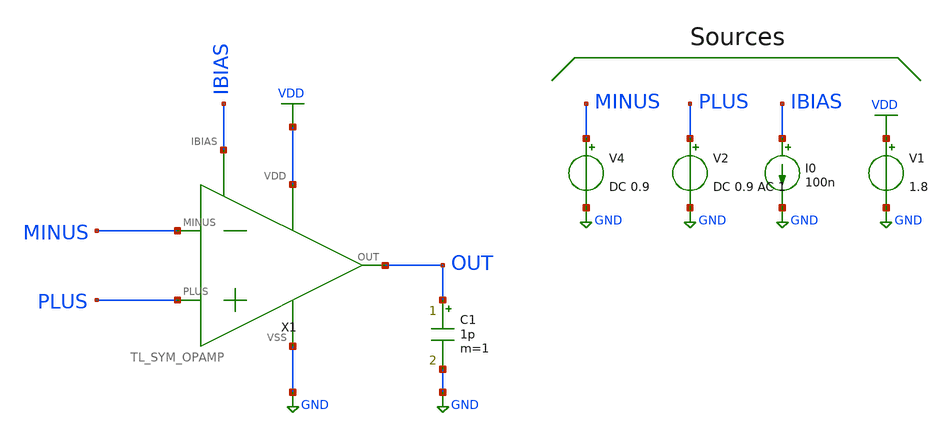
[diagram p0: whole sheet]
** sch_path: xschem/MISC/TB_DC_OPAMP.sch
**.subckt TB_DC_OPAMP
I0 IBIAS GND 100n
V1 VDD GND 1.8
V2 PLUS GND DC 0.9 AC 1
V4 MINUS GND DC 0.9
X1 PLUS MINUS OUT IBIAS GND VDD TL_SYM_OPAMP
C1 OUT GND 1p m=1
**** begin user architecture code



*.include ~/OpenPDK/skywater-pdk/skywater-pdk/libraries/sky130_fd_pr/latest/cells/pfet_g5v0d10v5/sky130_fd_pr__pfet_g5v0d10v5__tt.corner.spice
*.include ~/OpenPDK/skywater-pdk/skywater-pdk/libraries/sky130_fd_pr/latest/cells/pfet_g5v0d10v5/sky130_fd_pr__pfet_g5v0d10v5__mismatch.corner.spice
*.include ~/OpenPDK/skywater-pdk/skywater-pdk/libraries/sky130_fd_pr/latest/cells/pfet_g5v0d10v5/sky130_fd_pr__nfet_g5v0d10v5__tt.corner.spice
*.include ~/OpenPDK/skywater-pdk/skywater-pdk/libraries/sky130_fd_pr/latest/cells/pfet_g5v0d10v5/sky130_fd_pr__nfet_g5v0d10v5__mismatch.corner.spice

.include /usr/share/pdk/sky130A/libs.ref/spi/sky130_fd_pr/sky130_fd_pr__nfet_01v8_lvt__tt.corner.spice
.include /usr/share/pdk/sky130A/libs.ref/spi/sky130_fd_pr/sky130_fd_pr__nfet_01v8_lvt__mismatch.corner.spice
.include /usr/share/pdk/sky130A/libs.ref/spi/sky130_fd_pr/sky130_fd_pr__pfet_01v8_lvt__tt.corner.spice
.include /usr/share/pdk/sky130A/libs.ref/spi/sky130_fd_pr/sky130_fd_pr__pfet_01v8_lvt__mismatch.corner.spice

.include ~/OpenPDK/skywater-pdk/skywater-pdk/libraries/sky130_fd_pr/latest/models/all.spice





.option gmin=1E-21

.control

op
dc V2 0.85 0.95 10u
plot OUT
plot deriv(OUT)

ac dec 100 1 10MEG
plot db(OUT)

noise v(out) V2 dec 100 50m 100
print inoise_total
print onoise_total

.endc


**** end user architecture code
**.ends
.GLOBAL VDD
.GLOBAL GND
.end
